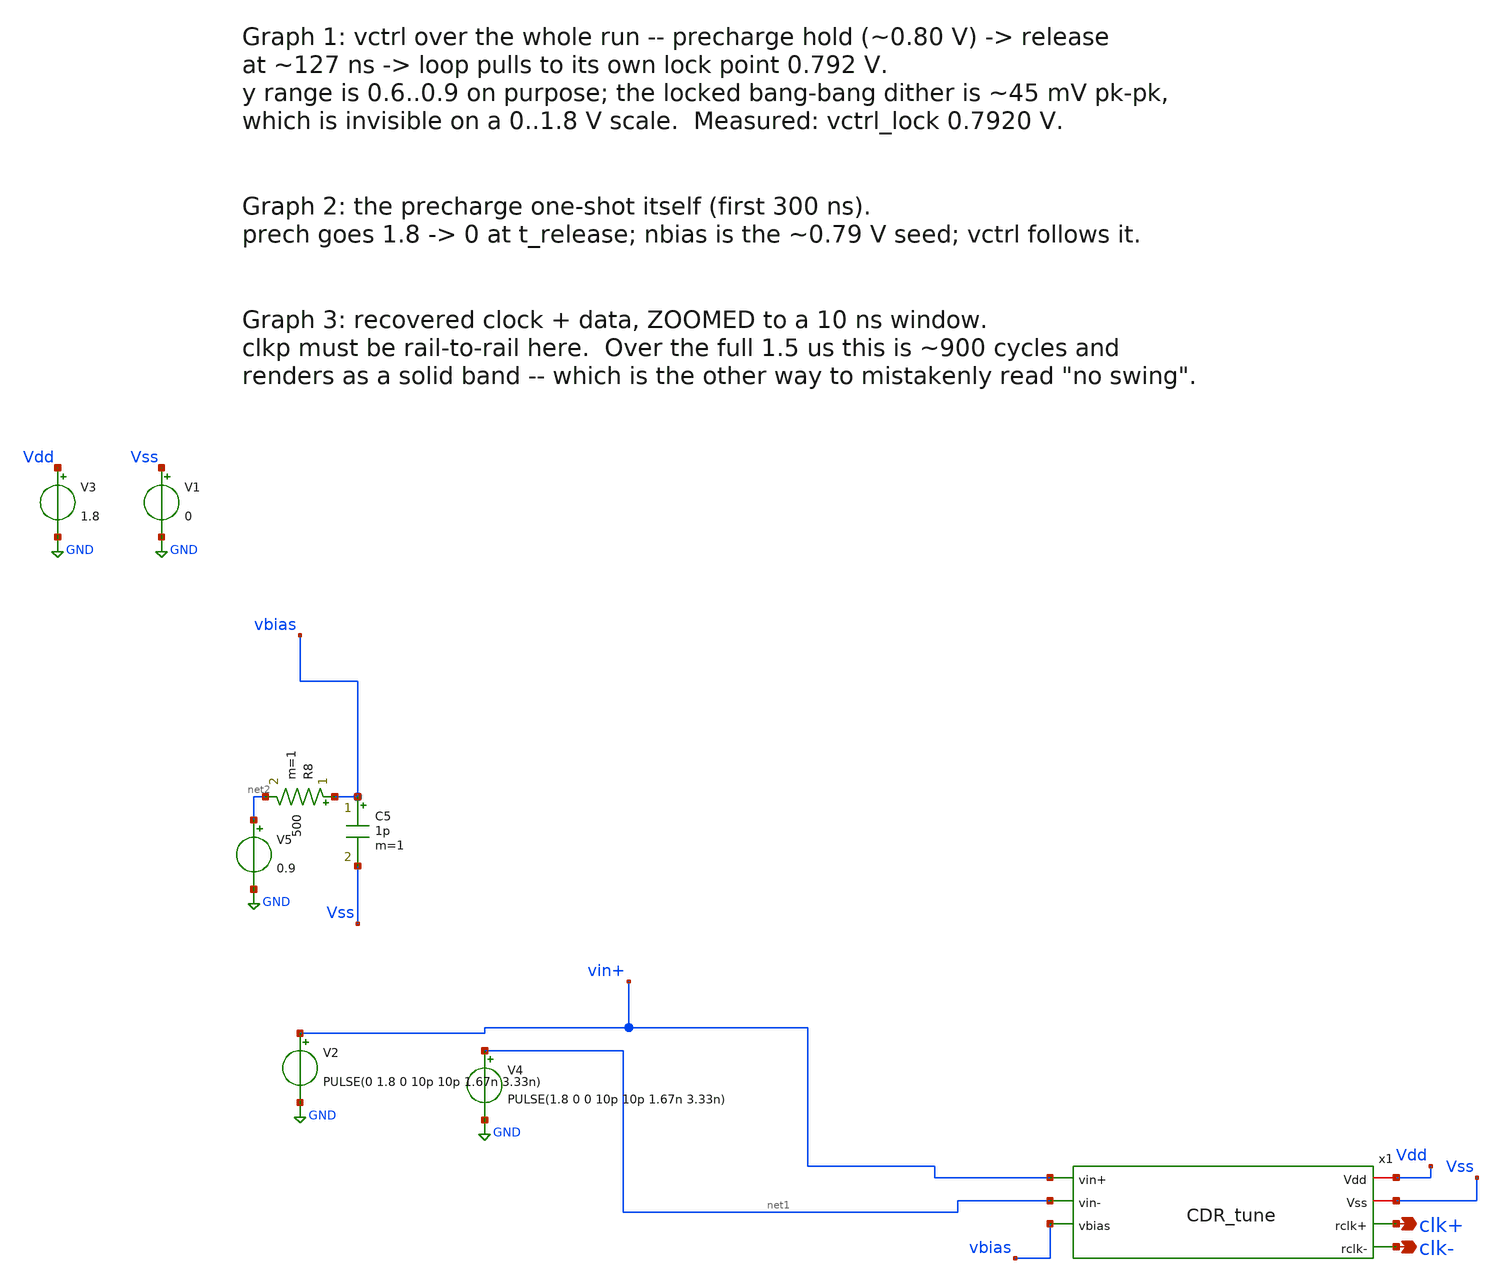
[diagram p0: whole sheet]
** sch_path: xschem/tuning/CDR_tune_tb.sch
**.subckt CDR_tune_tb clk- clk+
*.opin clk-
*.opin clk+
V3 Vdd GND 1.8
V1 Vss GND 0
V2 vin+ GND PULSE(0 1.8 0 10p 10p 1.67n 3.33n)
V4 net1 GND PULSE(1.8 0 0 10p 10p 1.67n 3.33n)
V5 net2 GND 0.9
R8 vbias net2 500 m=1
C5 vbias Vss 1p m=1
x1 Vdd Vss vin+ net1 vbias clk+ clk- CDR_tune
**** begin user architecture code



.lib /home/ttuser/pdk/sky130A/libs.tech/ngspice/sky130.lib.spice tt
.include /home/ttuser/pdk/sky130A/libs.ref/sky130_fd_sc_hd/spice/sky130_fd_sc_hd.spice
.options method=gear reltol=0.001 abstol=1e-12
* ---------------------------------------------------------------------------
* Plain-named copies of the two signals whose real names contain a '+'.
* `let clkp = v(clk+)` does NOT work: ngspice's expression parser reads the '+'
* as an operator and the assignment silently produces nothing (the vector just
* never appears in the .raw).  A unity VCVS sidesteps it -- a netlist line is
* plain tokens, no expression parsing -- and an ideal VCVS has infinite input
* impedance, so it cannot load the node it copies.
* ---------------------------------------------------------------------------
Eclkp  clkp  0 clk+ 0 1
Edatap datap 0 vin+ 0 1
* ---------------------------------------------------------------------------
* The startup precharge (x20) needs this ONE initial condition to work.
* .op treats a capacitor as an OPEN, so without it the POR node nrc solves to
* Vdd, `pre` sits at 0, the one-shot never fires and the cell is completely
* inert -- vctrl then seeds at ~0.663 V, right on the VCO dead-zone cliff.
* This is NOT a seed on vctrl: it just says the POR cap is discharged at
* power-up, which is physically true.  (See NOTES.md 17e.)
* ---------------------------------------------------------------------------
.ic v(x1.x20.nrc)=0
.op
.control
* `save` keeps the .raw small.  The bare `write` stored EVERY node of the whole
* CDR for 75000 timepoints, which is what OOM-crashed the VM.  Add nodes here
* if you want to probe something else.
  save v(x1.net1) v(clk+) v(clkp) v(datap) v(x1.x20.pre) v(x1.x20.nbias) v(x1.x20.nrc)
  tran 20p 1500n
* Hierarchical nodes are safe to alias with `let` (no '+' in the name); clkp and
* datap already exist as real nodes, courtesy of the two VCVS above.
  let vctrl = v(x1.net1)
  let prech = v(x1.x20.pre)
  let nbias = v(x1.x20.nbias)
  write CDR_tune_tb.raw
* --- numeric summary, printed in the ngspice log ---
  meas tran vctrl_lock AVG v(x1.net1) FROM=1300n TO=1400n
  meas tran vctrl_ripp PP  v(x1.net1) FROM=1300n TO=1400n
  meas tran clk_swing  PP  v(clk+)    FROM=1300n TO=1400n
  meas tran t_release  WHEN v(x1.x20.pre)=0.9 FALL=1
  meas tran c600 WHEN v(clk+)=0.9 RISE=600
  meas tran c660 WHEN v(clk+)=0.9 RISE=660
  let f_MHz = 60/(c660-c600)/1e6
  print f_MHz
.endc



**** end user architecture code
**.ends
.GLOBAL GND
.end
